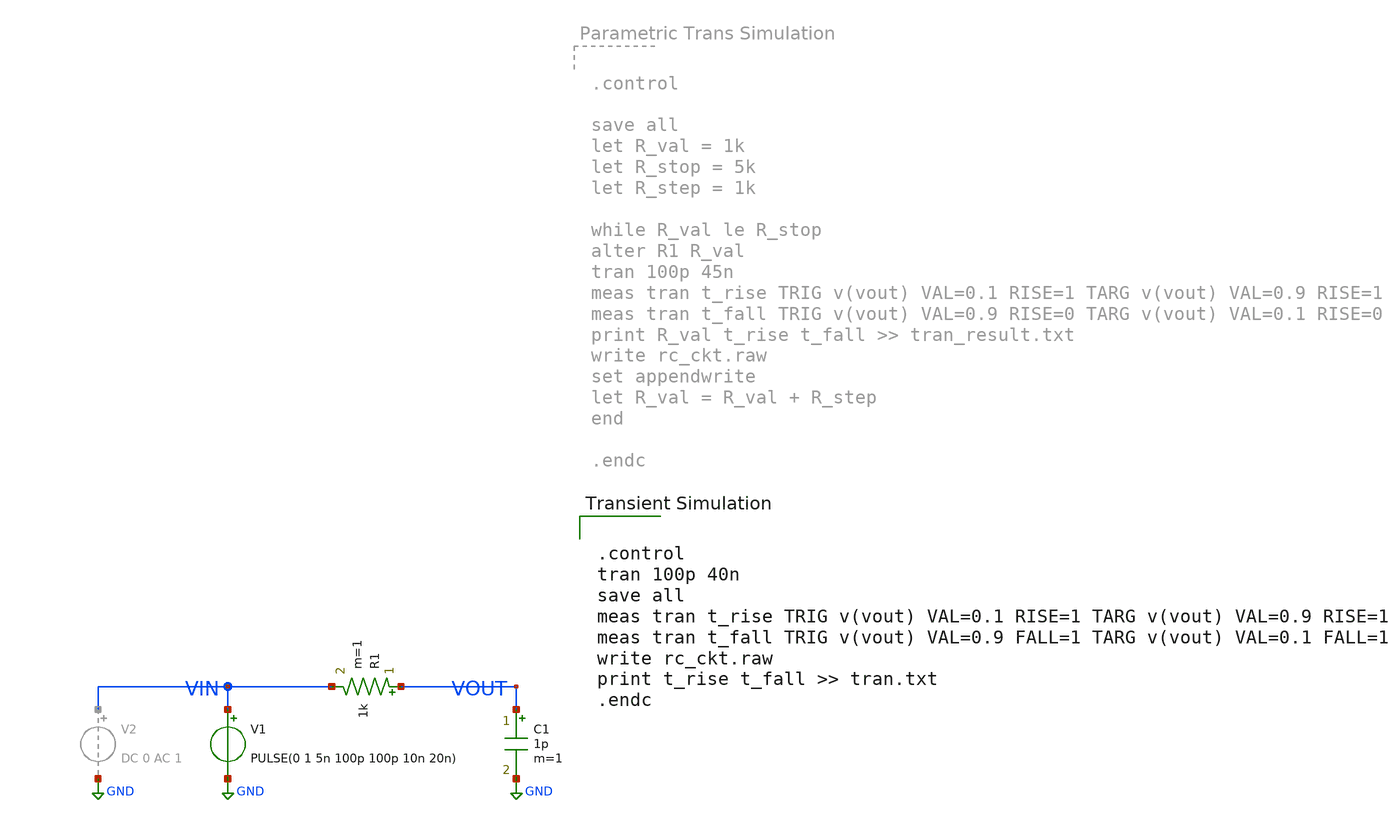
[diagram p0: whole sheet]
** sch_path: ITI_Labs/Lab1/RC/Design/RC.sch
**.subckt RC
C1 VOUT GND 1p m=1
R1 VOUT VIN 1k m=1
V1 VIN GND PULSE(0 1 5n 100p 100p 10n 20n)
**** begin user architecture code


.control
tran 100p 40n
save all
meas tran t_rise TRIG v(vout) VAL=0.1 RISE=1 TARG v(vout) VAL=0.9 RISE=1
meas tran t_fall TRIG v(vout) VAL=0.9 FALL=1 TARG v(vout) VAL=0.1 FALL=1
write rc_ckt.raw
print t_rise t_fall >> tran.txt
.endc


**** end user architecture code
**.ends
.GLOBAL GND
.end
